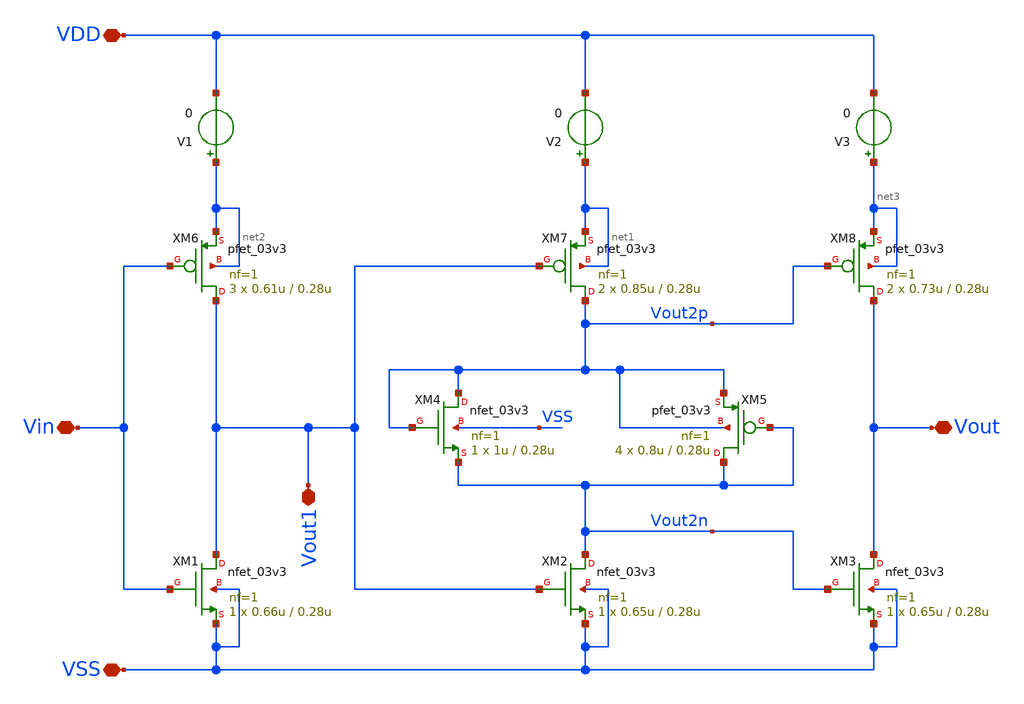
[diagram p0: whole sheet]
** sch_path: designs/DS_modulator/ring_amp/xschem/ring_amp.sch
**.subckt ring_amp VDD VSS Vin Vout Vout1
*.iopin VDD
*.iopin VSS
*.iopin Vin
*.iopin Vout
*.iopin Vout1
XM1 Vout1 Vin VSS VSS nfet_03v3 L=0.28u W=0.66u nf=1 ad='int((nf+1)/2) * W/nf * 0.18u' as='int((nf+2)/2) * W/nf * 0.18u'
+ pd='2*int((nf+1)/2) * (W/nf + 0.18u)' ps='2*int((nf+2)/2) * (W/nf + 0.18u)' nrd='0.18u / W' nrs='0.18u / W'
+ sa=0 sb=0 sd=0 m=1
XM4 Vout2p Vout2p Vout2n VSS nfet_03v3 L=0.28u W=1u nf=1 ad='int((nf+1)/2) * W/nf * 0.18u' as='int((nf+2)/2) * W/nf * 0.18u'
+ pd='2*int((nf+1)/2) * (W/nf + 0.18u)' ps='2*int((nf+2)/2) * (W/nf + 0.18u)' nrd='0.18u / W' nrs='0.18u / W'
+ sa=0 sb=0 sd=0 m=1
XM3 Vout Vout2n VSS VSS nfet_03v3 L=0.28u W=0.65u nf=1 ad='int((nf+1)/2) * W/nf * 0.18u' as='int((nf+2)/2) * W/nf * 0.18u'
+ pd='2*int((nf+1)/2) * (W/nf + 0.18u)' ps='2*int((nf+2)/2) * (W/nf + 0.18u)' nrd='0.18u / W' nrs='0.18u / W'
+ sa=0 sb=0 sd=0 m=1
XM5 Vout2n Vout2n Vout2p Vout2p pfet_03v3 L=0.28u W=0.8u nf=1 ad='int((nf+1)/2) * W/nf * 0.18u' as='int((nf+2)/2) * W/nf * 0.18u'
+ pd='2*int((nf+1)/2) * (W/nf + 0.18u)' ps='2*int((nf+2)/2) * (W/nf + 0.18u)' nrd='0.18u / W' nrs='0.18u / W'
+ sa=0 sb=0 sd=0 m=4
XM6 Vout1 Vin net2 net2 pfet_03v3 L=0.28u W=0.61u nf=1 ad='int((nf+1)/2) * W/nf * 0.18u' as='int((nf+2)/2) * W/nf * 0.18u'
+ pd='2*int((nf+1)/2) * (W/nf + 0.18u)' ps='2*int((nf+2)/2) * (W/nf + 0.18u)' nrd='0.18u / W' nrs='0.18u / W'
+ sa=0 sb=0 sd=0 m=3
XM8 Vout Vout2p net3 net3 pfet_03v3 L=0.28u W=0.73u nf=1 ad='int((nf+1)/2) * W/nf * 0.18u' as='int((nf+2)/2) * W/nf * 0.18u'
+ pd='2*int((nf+1)/2) * (W/nf + 0.18u)' ps='2*int((nf+2)/2) * (W/nf + 0.18u)' nrd='0.18u / W' nrs='0.18u / W'
+ sa=0 sb=0 sd=0 m=2
V1 net2 VDD 0
.save i(v1)
V2 net1 VDD 0
.save i(v2)
V3 net3 VDD 0
.save i(v3)
XM2 Vout2n Vout1 VSS VSS nfet_03v3 L=0.28u W=0.65u nf=1 ad='int((nf+1)/2) * W/nf * 0.18u' as='int((nf+2)/2) * W/nf * 0.18u'
+ pd='2*int((nf+1)/2) * (W/nf + 0.18u)' ps='2*int((nf+2)/2) * (W/nf + 0.18u)' nrd='0.18u / W' nrs='0.18u / W'
+ sa=0 sb=0 sd=0 m=1
XM7 Vout2p Vout1 net1 net1 pfet_03v3 L=0.28u W=0.85u nf=1 ad='int((nf+1)/2) * W/nf * 0.18u' as='int((nf+2)/2) * W/nf * 0.18u'
+ pd='2*int((nf+1)/2) * (W/nf + 0.18u)' ps='2*int((nf+2)/2) * (W/nf + 0.18u)' nrd='0.18u / W' nrs='0.18u / W'
+ sa=0 sb=0 sd=0 m=2
**.ends
.end
